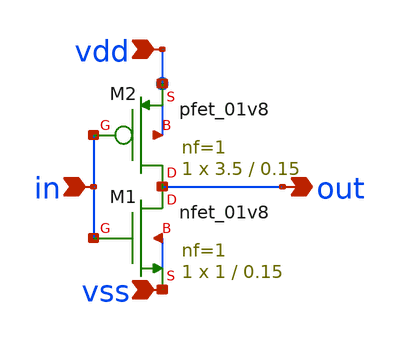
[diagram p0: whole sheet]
** sch_path: custom_gds/tt_um_tim2305_adc_dac/xschem/sti.sch
**.subckt sti in vss vdd out
*.ipin in
*.ipin vss
*.ipin vdd
*.opin out
XM1 out in vss vss sky130_fd_pr__nfet_01v8 L=0.15 W=1 nf=1 ad='int((nf+1)/2) * W/nf * 0.29' as='int((nf+2)/2) * W/nf * 0.29'
+ pd='2*int((nf+1)/2) * (W/nf + 0.29)' ps='2*int((nf+2)/2) * (W/nf + 0.29)' nrd='0.29 / W' nrs='0.29 / W'
+ sa=0 sb=0 sd=0 mult=1 m=1
XM2 out in vdd vdd sky130_fd_pr__pfet_01v8 L=0.15 W=3.5 nf=1 ad='int((nf+1)/2) * W/nf * 0.29' as='int((nf+2)/2) * W/nf * 0.29'
+ pd='2*int((nf+1)/2) * (W/nf + 0.29)' ps='2*int((nf+2)/2) * (W/nf + 0.29)' nrd='0.29 / W' nrs='0.29 / W'
+ sa=0 sb=0 sd=0 mult=1 m=1
**.ends
.end
